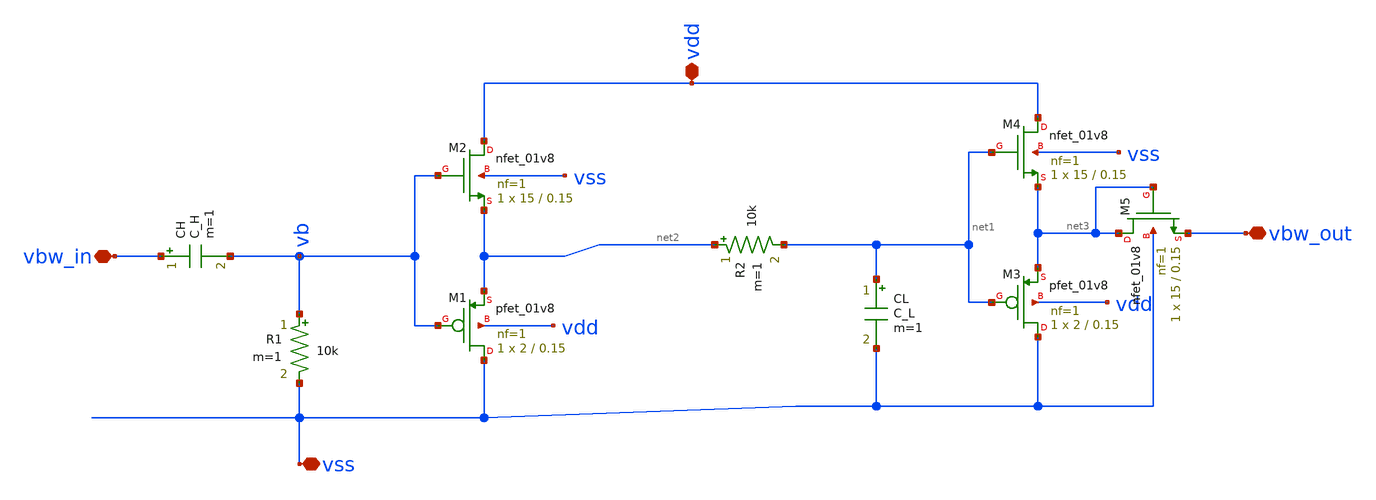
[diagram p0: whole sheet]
** sch_path: Synapse/bpfilter.sch
**.subckt bpfilter vbw_in vbw_out vss vdd
*.iopin vbw_in
*.iopin vbw_out
*.iopin vss
*.iopin vdd
R1 vb vss 10k m=1
R2 net2 net1 10k m=1
CL net1 vss C_L m=1
CH vbw_in vb C_H m=1
XM3 vss net1 net3 vdd sky130_fd_pr__pfet_01v8 L=0.15 W=2 nf=1 ad='int((nf+1)/2) * W/nf * 0.29' as='int((nf+2)/2) * W/nf * 0.29'
+ pd='2*int((nf+1)/2) * (W/nf + 0.29)' ps='2*int((nf+2)/2) * (W/nf + 0.29)' nrd='0.29 / W' nrs='0.29 / W'
+ sa=0 sb=0 sd=0 mult=1 m=1
XM4 vdd net1 net3 vss sky130_fd_pr__nfet_01v8 L=0.15 W=15 nf=1 ad='int((nf+1)/2) * W/nf * 0.29' as='int((nf+2)/2) * W/nf * 0.29'
+ pd='2*int((nf+1)/2) * (W/nf + 0.29)' ps='2*int((nf+2)/2) * (W/nf + 0.29)' nrd='0.29 / W' nrs='0.29 / W'
+ sa=0 sb=0 sd=0 mult=1 m=1
XM5 net3 net3 vbw_out vss sky130_fd_pr__nfet_01v8 L=0.15 W=15 nf=1 ad='int((nf+1)/2) * W/nf * 0.29' as='int((nf+2)/2) * W/nf * 0.29'
+ pd='2*int((nf+1)/2) * (W/nf + 0.29)' ps='2*int((nf+2)/2) * (W/nf + 0.29)' nrd='0.29 / W' nrs='0.29 / W'
+ sa=0 sb=0 sd=0 mult=1 m=1
XM1 vss vb net2 vdd sky130_fd_pr__pfet_01v8 L=0.15 W=2 nf=1 ad='int((nf+1)/2) * W/nf * 0.29' as='int((nf+2)/2) * W/nf * 0.29'
+ pd='2*int((nf+1)/2) * (W/nf + 0.29)' ps='2*int((nf+2)/2) * (W/nf + 0.29)' nrd='0.29 / W' nrs='0.29 / W'
+ sa=0 sb=0 sd=0 mult=1 m=1
XM2 vdd vb net2 vss sky130_fd_pr__nfet_01v8 L=0.15 W=15 nf=1 ad='int((nf+1)/2) * W/nf * 0.29' as='int((nf+2)/2) * W/nf * 0.29'
+ pd='2*int((nf+1)/2) * (W/nf + 0.29)' ps='2*int((nf+2)/2) * (W/nf + 0.29)' nrd='0.29 / W' nrs='0.29 / W'
+ sa=0 sb=0 sd=0 mult=1 m=1
**.ends
.end
